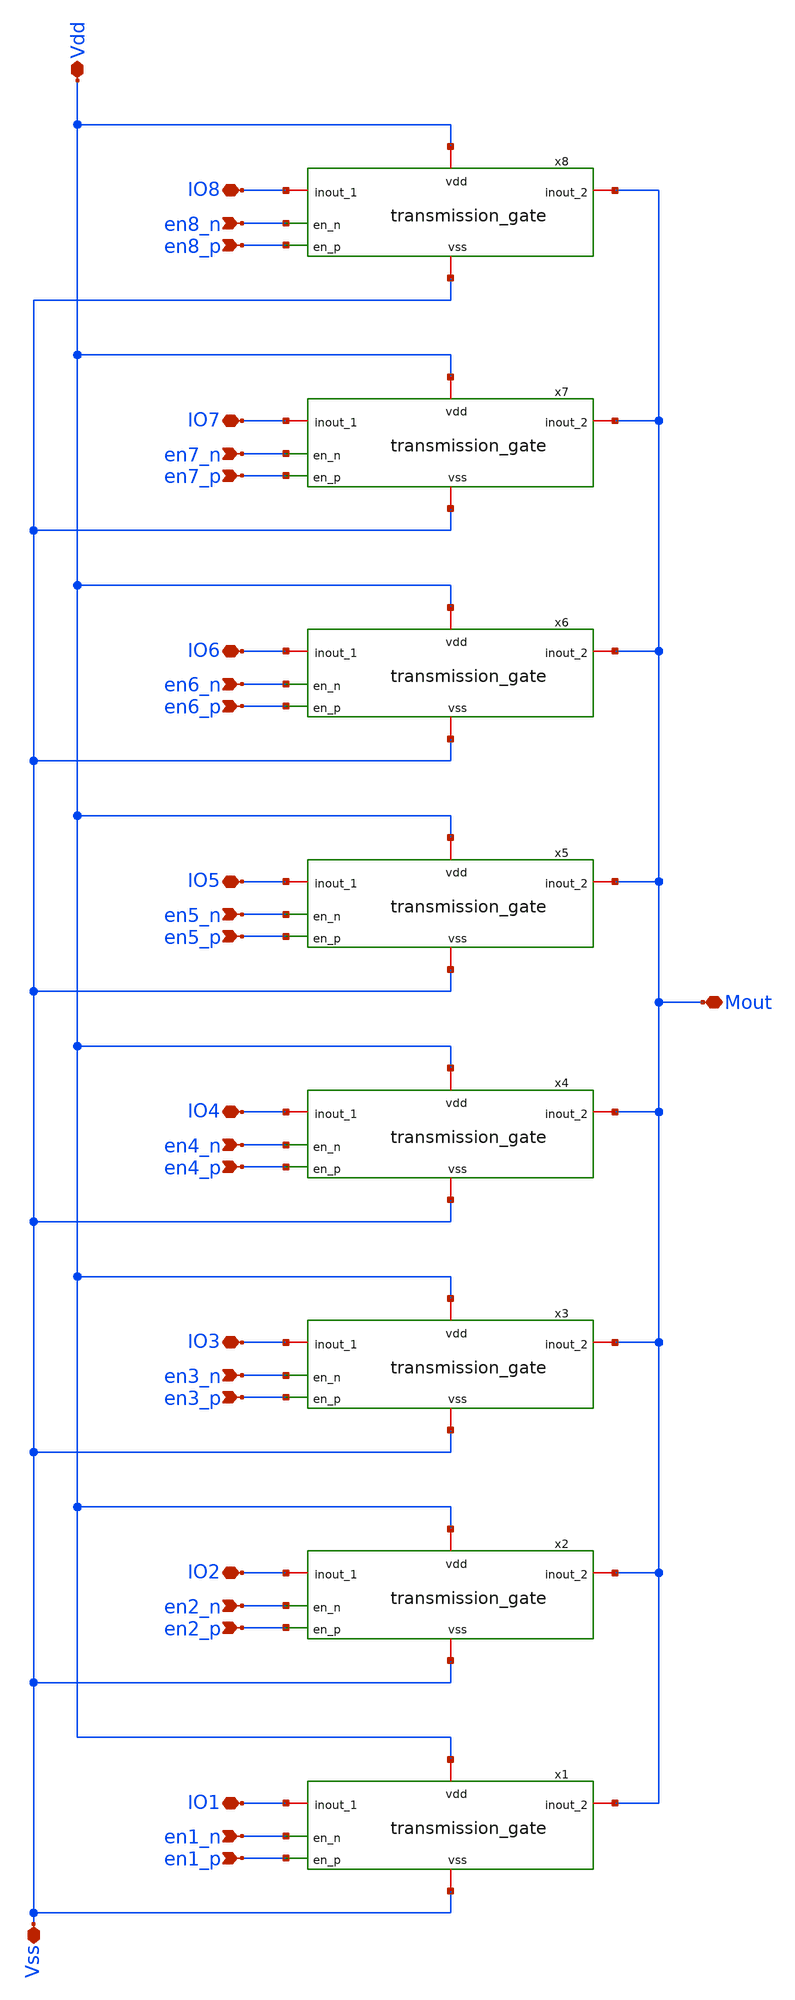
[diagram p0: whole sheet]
** sch_path: CHIPCHILE_CANELOS24_WorkshopTO/design_data/xschem/multiplexer/multiplexer.sch
* Copyright 2023 IHP PDK Authors
**.subckt multiplexer IO1 Vss en1_n en1_p IO2 Mout en2_n en2_p IO3 en3_n en3_p IO4 en4_n en4_p IO5
*+ en5_n en5_p IO6 en6_n en6_p IO7 en7_n en7_p IO8 Vdd en8_n en8_p
*.iopin IO1
*.iopin Vss
*.ipin en1_n
*.ipin en1_p
*.iopin IO2
*.iopin Mout
*.ipin en2_n
*.ipin en2_p
*.iopin IO3
*.ipin en3_n
*.ipin en3_p
*.iopin IO4
*.ipin en4_n
*.ipin en4_p
*.iopin IO5
*.ipin en5_n
*.ipin en5_p
*.iopin IO6
*.ipin en6_n
*.ipin en6_p
*.iopin IO7
*.ipin en7_n
*.ipin en7_p
*.iopin IO8
*.iopin Vdd
*.ipin en8_n
*.ipin en8_p
x1 Vdd en1_n IO1 Mout en1_p Vss transmission_gate
x2 Vdd en2_n IO2 Mout en2_p Vss transmission_gate
x3 Vdd en3_n IO3 Mout en3_p Vss transmission_gate
x4 Vdd en4_n IO4 Mout en4_p Vss transmission_gate
x5 Vdd en5_n IO5 Mout en5_p Vss transmission_gate
x6 Vdd en6_n IO6 Mout en6_p Vss transmission_gate
x7 Vdd en7_n IO7 Mout en7_p Vss transmission_gate
x8 Vdd en8_n IO8 Mout en8_p Vss transmission_gate
**.ends

* expanding   symbol:  transmission_gate.sym # of pins=6
** sym_path: CHIPCHILE_CANELOS24_WorkshopTO/design_data/xschem/multiplexer/transmission_gate.sym
** sch_path: CHIPCHILE_CANELOS24_WorkshopTO/design_data/xschem/multiplexer/transmission_gate.sch
.subckt transmission_gate vdd en_n inout_1 inout_2 en_p vss
*.iopin inout_1
*.iopin inout_2
*.ipin en_p
*.iopin vdd
*.iopin vss
*.ipin en_n
XM1 inout_1 en_p inout_2 net1 sg13_lv_nmos w=200.0u l=0.130u ng=20 m=1 mm_ok=1
XM2 inout_1 en_n inout_2 net2 sg13_lv_pmos w=200.0u l=0.130u ng=20 m=1 mm_ok=1
XR1 vdd net2 ntap1 R=262.8 w=0.78e-6 l=0.78e-6
XR2 vss net1 ptap1 R=262.8 w=0.78e-6 l=0.78e-6
.ends

.end
